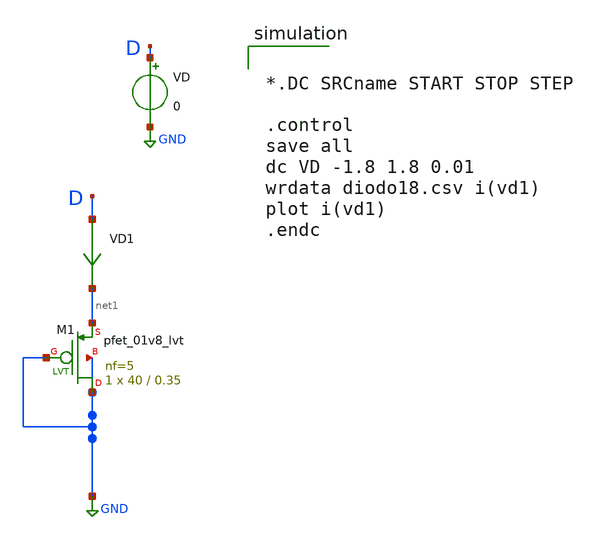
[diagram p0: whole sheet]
** sch_path: xschem/diodo-I-V-pnp.sch
**.subckt diodo-I-V-pnp
XM1 GND GND net1 GND sky130_fd_pr__pfet_01v8_lvt L=0.35 W=40 nf=5 ad='int((5 + 1)/2) * 40 / 5 * 0.29'
+ as='int((5 + 2)/2) * 40 / 5 * 0.29' pd='2*int((5 + 1)/2) * (40 / 5 + 0.29)' ps='2*int((5 + 2)/2) * (40 / 5 + 0.29)'
+ nrd='0.29 / 40 ' nrs='0.29 / 40 ' sa=0 sb=0 sd=0 mult=1 m=1
VD D GND 0
VD1 D net1 0
.save i(vd1)
**** begin user architecture code

** opencircuitdesign pdks install
.lib $::SKYWATER_MODELS/sky130.lib.spice tt




*.DC SRCname START STOP STEP

.control
save all
dc VD -1.8 1.8 0.01
wrdata diodo18.csv i(vd1)
plot i(vd1)
.endc



**** end user architecture code
**.ends
.GLOBAL GND
.end
